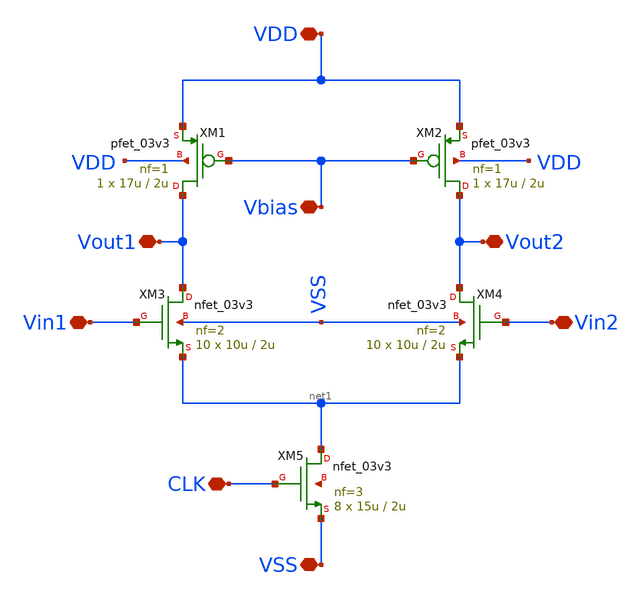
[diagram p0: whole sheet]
** sch_path: designs/comparator/preamp/preamp.sch
**.subckt preamp VSS VDD Vout1 Vout2 Vin1 Vin2 CLK Vbias
*.iopin VSS
*.iopin VDD
*.iopin Vout1
*.iopin Vout2
*.iopin Vin1
*.iopin Vin2
*.iopin CLK
*.iopin Vbias
XM1 Vout1 Vbias VDD VDD pfet_03v3 L=2u W=17u nf=1 ad='int((nf+1)/2) * W/nf * 0.18u' as='int((nf+2)/2) * W/nf * 0.18u'
+ pd='2*int((nf+1)/2) * (W/nf + 0.18u)' ps='2*int((nf+2)/2) * (W/nf + 0.18u)' nrd='0.18u / W' nrs='0.18u / W'
+ sa=0 sb=0 sd=0 m=1
XM2 Vout2 Vbias VDD VDD pfet_03v3 L=2u W=17u nf=1 ad='int((nf+1)/2) * W/nf * 0.18u' as='int((nf+2)/2) * W/nf * 0.18u'
+ pd='2*int((nf+1)/2) * (W/nf + 0.18u)' ps='2*int((nf+2)/2) * (W/nf + 0.18u)' nrd='0.18u / W' nrs='0.18u / W'
+ sa=0 sb=0 sd=0 m=1
XM3 Vout1 Vin1 net1 VSS nfet_03v3 L=2u W=10u nf=2 ad='int((nf+1)/2) * W/nf * 0.18u' as='int((nf+2)/2) * W/nf * 0.18u'
+ pd='2*int((nf+1)/2) * (W/nf + 0.18u)' ps='2*int((nf+2)/2) * (W/nf + 0.18u)' nrd='0.18u / W' nrs='0.18u / W'
+ sa=0 sb=0 sd=0 m=10
XM4 Vout2 Vin2 net1 VSS nfet_03v3 L=2u W=10u nf=2 ad='int((nf+1)/2) * W/nf * 0.18u' as='int((nf+2)/2) * W/nf * 0.18u'
+ pd='2*int((nf+1)/2) * (W/nf + 0.18u)' ps='2*int((nf+2)/2) * (W/nf + 0.18u)' nrd='0.18u / W' nrs='0.18u / W'
+ sa=0 sb=0 sd=0 m=10
XM5 net1 CLK VSS net2 nfet_03v3 L=2u W=15u nf=3 ad='int((nf+1)/2) * W/nf * 0.18u' as='int((nf+2)/2) * W/nf * 0.18u'
+ pd='2*int((nf+1)/2) * (W/nf + 0.18u)' ps='2*int((nf+2)/2) * (W/nf + 0.18u)' nrd='0.18u / W' nrs='0.18u / W'
+ sa=0 sb=0 sd=0 m=8
**.ends
.end
